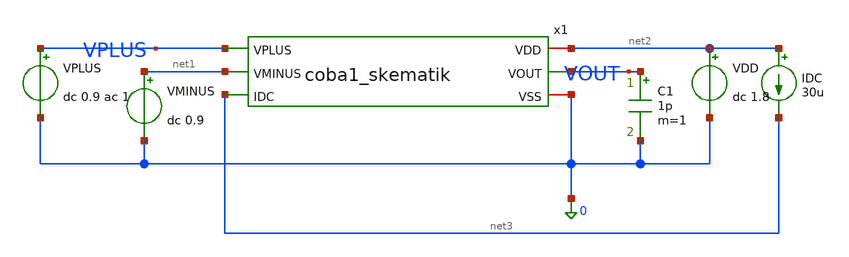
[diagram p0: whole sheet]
** sch_path: coba1_skematik_tb.sch
**.subckt coba1_skematik_tb
VDD net2 0 dc 1.8
VPLUS VPLUS 0 dc 0.9 ac 1
VMINUS net1 0 dc 0.9
IDC net2 net3 30u
C1 VOUT 0 1p m=1
x1 net2 VOUT VPLUS net1 net3 0 coba1_skematik
**** begin user architecture code


.lib /foss/pdks/sky130A/libs.tech/ngspice/sky130.lib.spice tt
.ac dec 20 1 100Meg
.save all
.control
run
let open_loop_gain = v(VOUT)/v(VPLUS)
plot db(open_loop_gain) xlog
plot ph(open_loop_gain) xlog
.endc


**** end user architecture code
**.ends

* expanding   symbol:  /foss/designs/kelompok4/coba1_skematik.sym # of pins=6
** sym_path: coba1_skematik.sym
** sch_path: coba1_skematik.sch
.subckt coba1_skematik VDD VOUT VPLUS VMINUS IDC VSS
*.ipin VPLUS
*.ipin VMINUS
*.ipin IDC
*.opin VOUT
*.iopin VDD
*.iopin VSS
XM1 net1 net1 VDD VDD sky130_fd_pr__pfet_01v8 L=1 W=15 nf=3 ad='int((3 + 1)/2) * 15 / 3 * 0.29' as='int((3 + 2)/2) * 15 / 3 * 0.29'
+ pd='2*int((3 + 1)/2) * (15 / 3 + 0.29)' ps='2*int((3 + 2)/2) * (15 / 3 + 0.29)' nrd='0.29 / 15 ' nrs='0.29 / 15 '
+ sa=0 sb=0 sd=0 mult=1 m=1
XM2 net2 net1 VDD VDD sky130_fd_pr__pfet_01v8 L=1 W=15 nf=3 ad='int((3 + 1)/2) * 15 / 3 * 0.29' as='int((3 + 2)/2) * 15 / 3 * 0.29'
+ pd='2*int((3 + 1)/2) * (15 / 3 + 0.29)' ps='2*int((3 + 2)/2) * (15 / 3 + 0.29)' nrd='0.29 / 15 ' nrs='0.29 / 15 '
+ sa=0 sb=0 sd=0 mult=1 m=1
XM3 net1 VMINUS net3 VSS sky130_fd_pr__nfet_01v8 L=1 W=30 nf=6 ad='int((6 + 1)/2) * 30 / 6 * 0.29' as='int((6 + 2)/2) * 30 / 6 * 0.29'
+ pd='2*int((6 + 1)/2) * (30 / 6 + 0.29)' ps='2*int((6 + 2)/2) * (30 / 6 + 0.29)' nrd='0.29 / 30 ' nrs='0.29 / 30 '
+ sa=0 sb=0 sd=0 mult=1 m=1
XM4 net2 VPLUS net3 VSS sky130_fd_pr__nfet_01v8 L=1 W=30 nf=6 ad='int((6 + 1)/2) * 30 / 6 * 0.29' as='int((6 + 2)/2) * 30 / 6 * 0.29'
+ pd='2*int((6 + 1)/2) * (30 / 6 + 0.29)' ps='2*int((6 + 2)/2) * (30 / 6 + 0.29)' nrd='0.29 / 30 ' nrs='0.29 / 30 '
+ sa=0 sb=0 sd=0 mult=1 m=1
XM5 net3 IDC VSS VSS sky130_fd_pr__nfet_01v8 L=1 W=4.5 nf=1 ad='int((1 + 1)/2) * 4.5 / 1 * 0.29' as='int((1 + 2)/2) * 4.5 / 1 * 0.29'
+ pd='2*int((1 + 1)/2) * (4.5 / 1 + 0.29)' ps='2*int((1 + 2)/2) * (4.5 / 1 + 0.29)' nrd='0.29 / 4.5 ' nrs='0.29 / 4.5 '
+ sa=0 sb=0 sd=0 mult=1 m=1
XM6 IDC IDC VSS VSS sky130_fd_pr__nfet_01v8 L=1 W=4.5 nf=1 ad='int((1 + 1)/2) * 4.5 / 1 * 0.29' as='int((1 + 2)/2) * 4.5 / 1 * 0.29'
+ pd='2*int((1 + 1)/2) * (4.5 / 1 + 0.29)' ps='2*int((1 + 2)/2) * (4.5 / 1 + 0.29)' nrd='0.29 / 4.5 ' nrs='0.29 / 4.5 '
+ sa=0 sb=0 sd=0 mult=1 m=1
XM7 VOUT net2 VDD VDD sky130_fd_pr__pfet_01v8 L=1 W=30 nf=6 ad='int((6 + 1)/2) * 30 / 6 * 0.29' as='int((6 + 2)/2) * 30 / 6 * 0.29'
+ pd='2*int((6 + 1)/2) * (30 / 6 + 0.29)' ps='2*int((6 + 2)/2) * (30 / 6 + 0.29)' nrd='0.29 / 30 ' nrs='0.29 / 30 '
+ sa=0 sb=0 sd=0 mult=1 m=1
XM8 VOUT IDC VSS VSS sky130_fd_pr__nfet_01v8 L=1 W=4.5 nf=1 ad='int((1 + 1)/2) * 4.5 / 1 * 0.29' as='int((1 + 2)/2) * 4.5 / 1 * 0.29'
+ pd='2*int((1 + 1)/2) * (4.5 / 1 + 0.29)' ps='2*int((1 + 2)/2) * (4.5 / 1 + 0.29)' nrd='0.29 / 4.5 ' nrs='0.29 / 4.5 '
+ sa=0 sb=0 sd=0 mult=1 m=1
C1 net2 VOUT 1p m=1
.ends

.end
